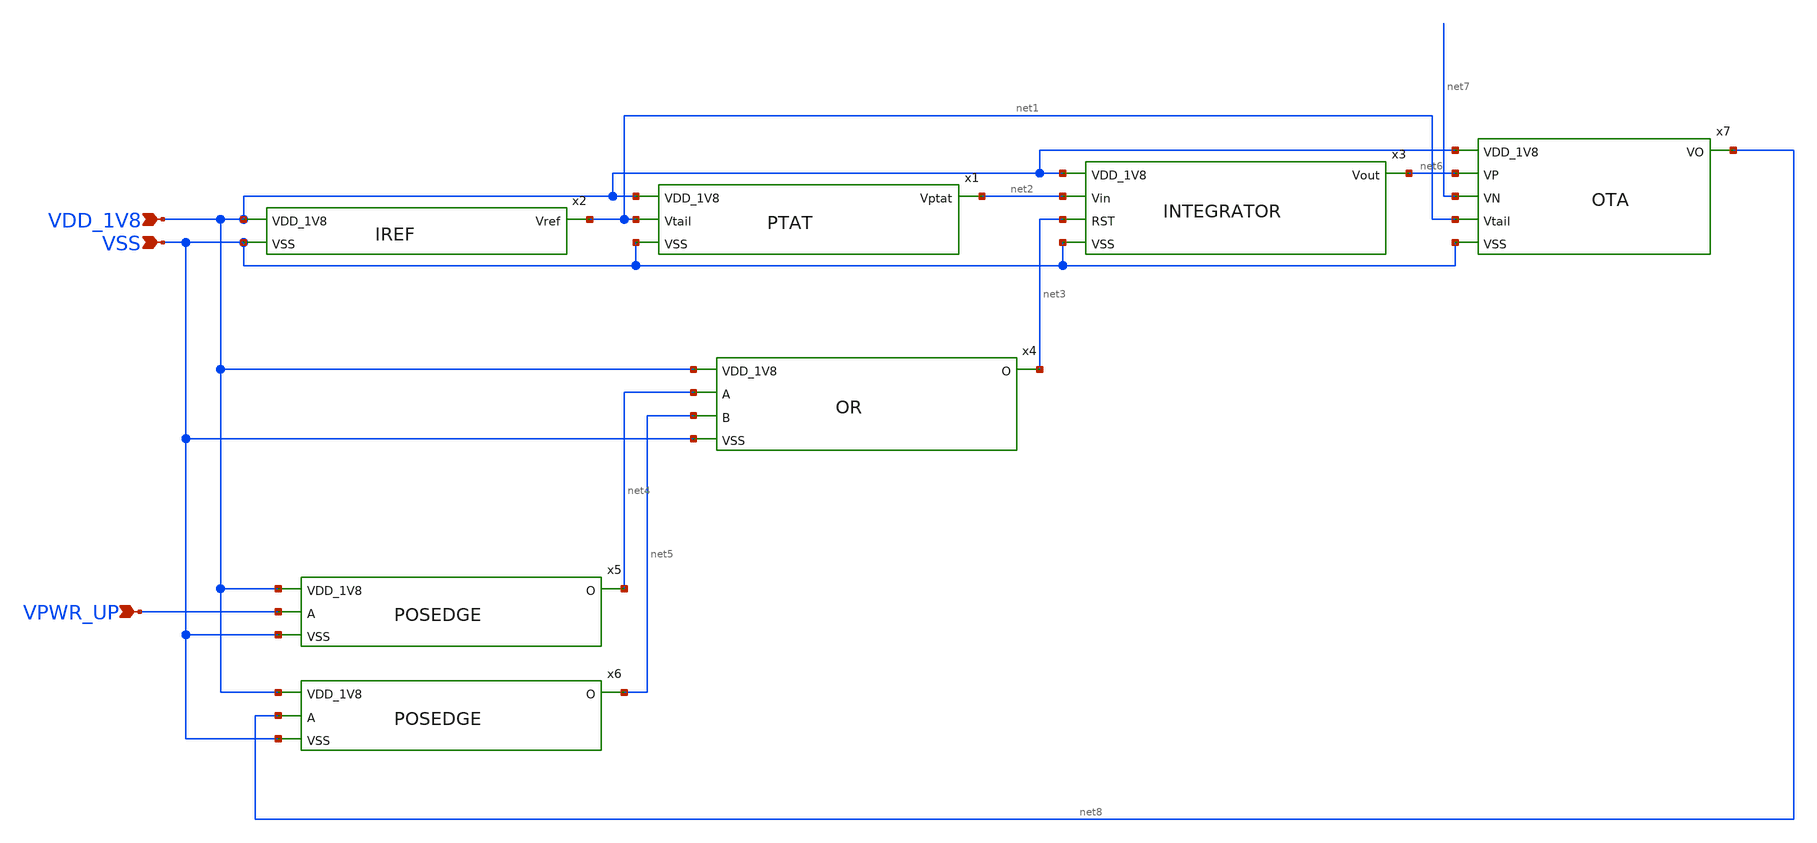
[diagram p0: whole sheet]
** sch_path: design/CNR_GR05_SKY130NM/final.sch
**.subckt final VDD_1V8 VSS VPWR_UP
*.ipin VDD_1V8
*.ipin VSS
*.ipin VPWR_UP
x1 VDD_1V8 net1 VSS net2 PTAT
x2 VDD_1V8 net1 VSS IREF
x3 VDD_1V8 net2 net6 net3 VSS INTEGRATOR
x4 VDD_1V8 net4 net5 net3 VSS OR
x5 VDD_1V8 VPWR_UP net4 VSS POSEDGE
x6 VDD_1V8 net8 net5 VSS POSEDGE
x7 VDD_1V8 net8 net6 net7 net1 VSS OTA
**.ends
.end
